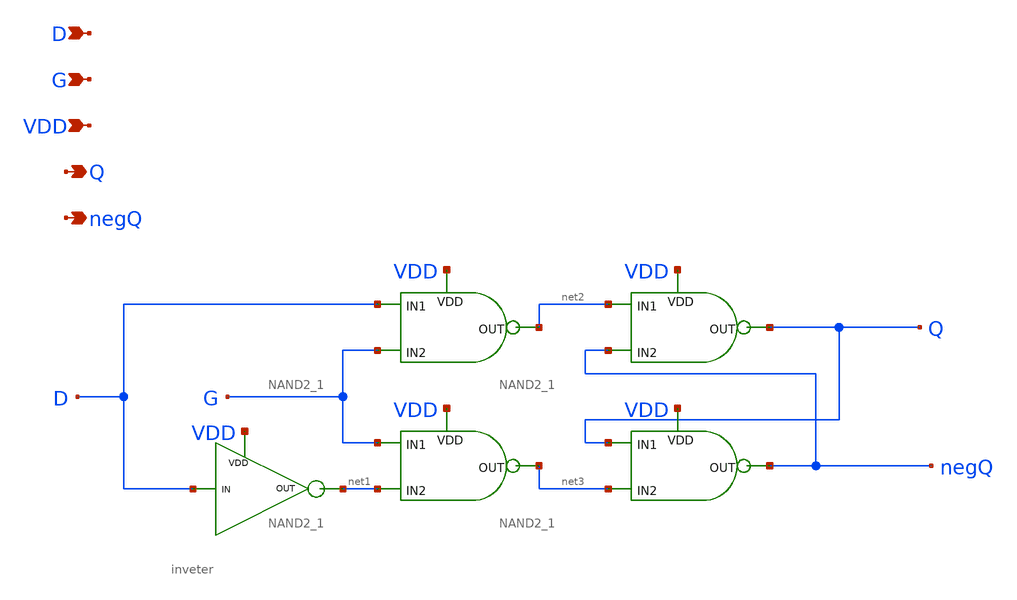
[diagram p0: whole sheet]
** sch_path: initial_notebooks_2023/Current-Steering DAC/DLatch.sch
**.subckt DLatch D VDD G Q negQ
*.ipin D
*.ipin VDD
*.ipin G
*.opin Q
*.opin negQ
x5 VDD net1 D inveter
x1 VDD D net2 G NAND2_1
x3 VDD net2 Q negQ NAND2_1
x2 VDD G net3 net1 NAND2_1
x4 VDD Q negQ net3 NAND2_1
**.ends
.end
